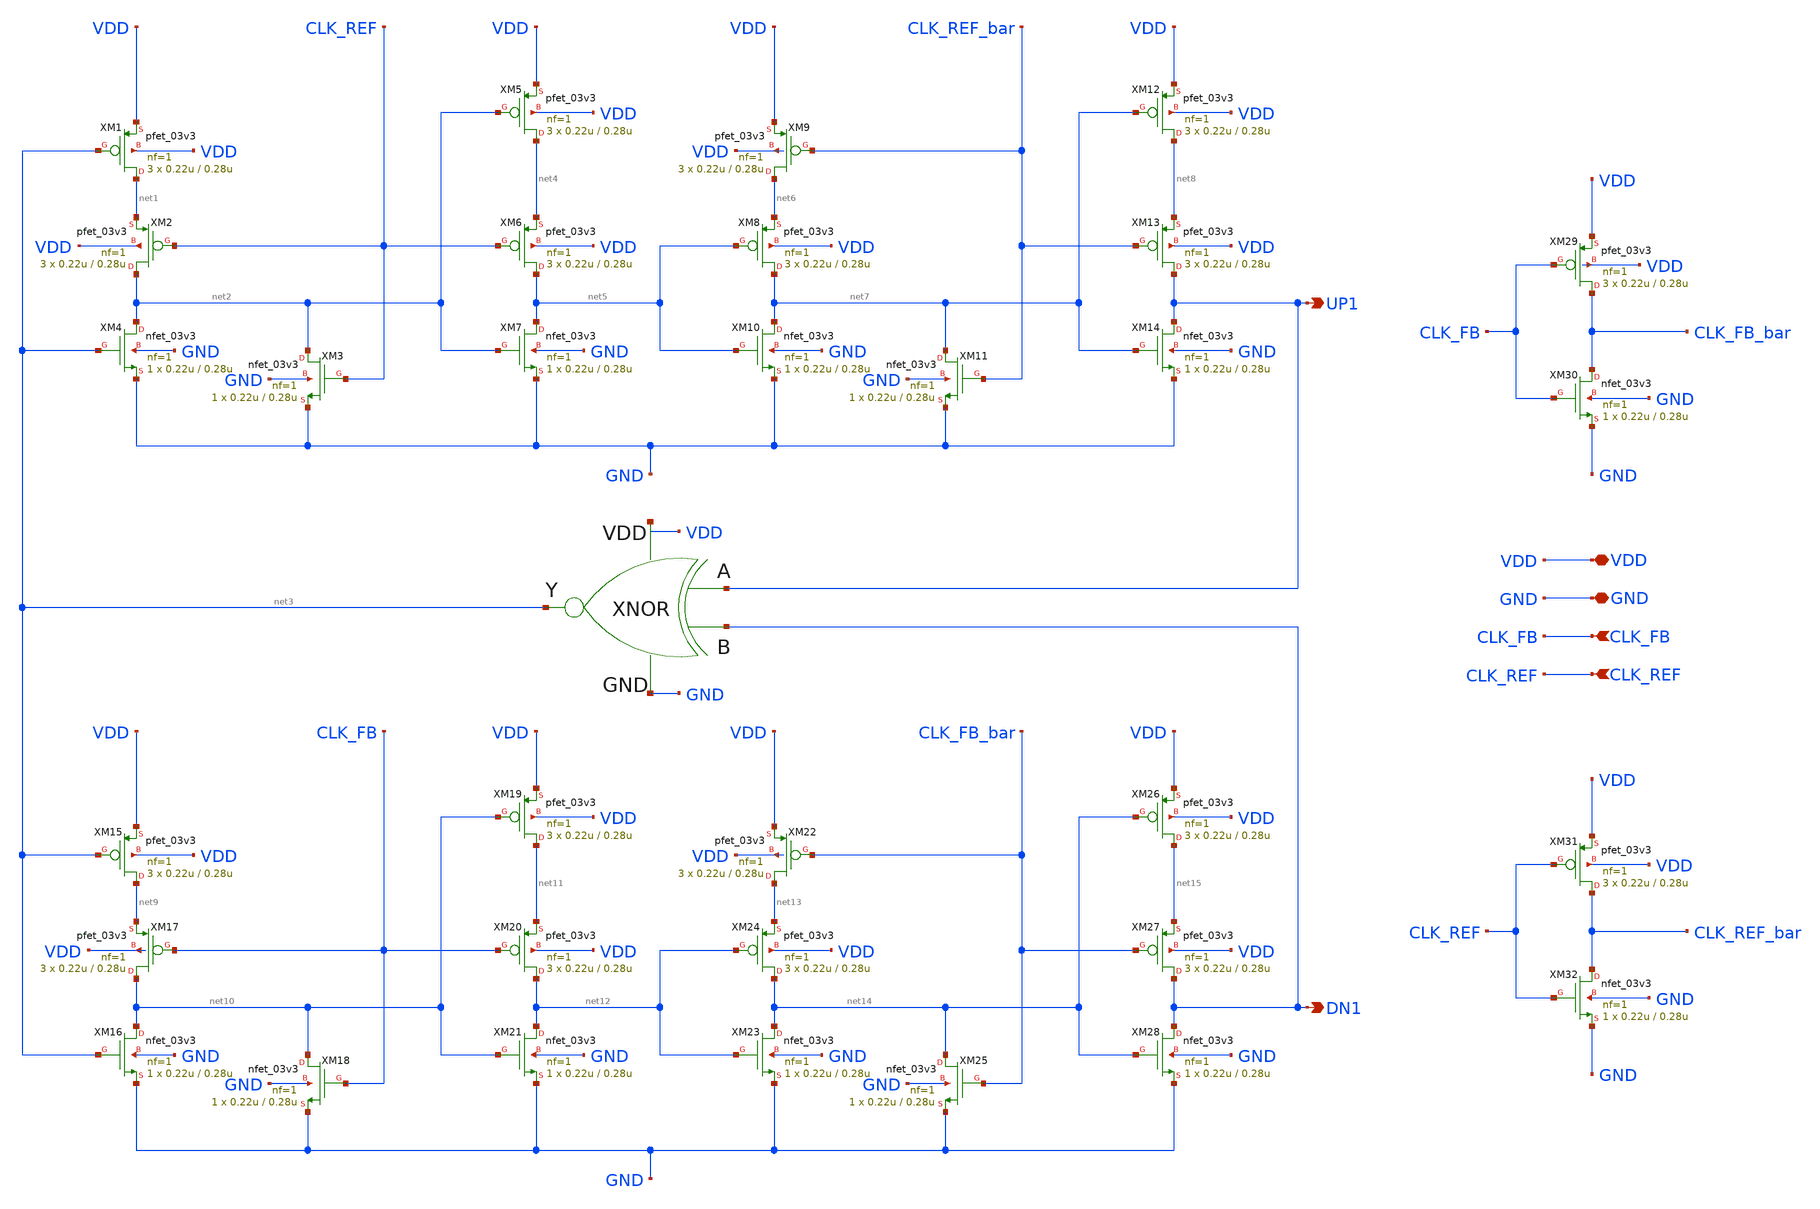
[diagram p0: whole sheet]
** sch_path: PFD/FTL_PFD.sch
**.subckt FTL_PFD UP1 DN1 CLK_FB CLK_REF VDD GND
*.opin UP1
*.opin DN1
*.ipin CLK_FB
*.ipin CLK_REF
*.iopin VDD
*.iopin GND
XM1 net1 net3 VDD VDD pfet_03v3 L=0.28u W=0.22u nf=1 ad='int((nf+1)/2) * W/nf * 0.18u' as='int((nf+2)/2) * W/nf * 0.18u'
+ pd='2*int((nf+1)/2) * (W/nf + 0.18u)' ps='2*int((nf+2)/2) * (W/nf + 0.18u)' nrd='0.18u / W' nrs='0.18u / W'
+ sa=0 sb=0 sd=0 m=3
XM4 net2 net3 GND GND nfet_03v3 L=0.28u W=0.22u nf=1 ad='int((nf+1)/2) * W/nf * 0.18u' as='int((nf+2)/2) * W/nf * 0.18u'
+ pd='2*int((nf+1)/2) * (W/nf + 0.18u)' ps='2*int((nf+2)/2) * (W/nf + 0.18u)' nrd='0.18u / W' nrs='0.18u / W'
+ sa=0 sb=0 sd=0 m=1
XM2 net2 CLK_REF net1 VDD pfet_03v3 L=0.28u W=0.22u nf=1 ad='int((nf+1)/2) * W/nf * 0.18u' as='int((nf+2)/2) * W/nf * 0.18u'
+ pd='2*int((nf+1)/2) * (W/nf + 0.18u)' ps='2*int((nf+2)/2) * (W/nf + 0.18u)' nrd='0.18u / W' nrs='0.18u / W'
+ sa=0 sb=0 sd=0 m=3
XM3 net2 CLK_REF GND GND nfet_03v3 L=0.28u W=0.22u nf=1 ad='int((nf+1)/2) * W/nf * 0.18u' as='int((nf+2)/2) * W/nf * 0.18u'
+ pd='2*int((nf+1)/2) * (W/nf + 0.18u)' ps='2*int((nf+2)/2) * (W/nf + 0.18u)' nrd='0.18u / W' nrs='0.18u / W'
+ sa=0 sb=0 sd=0 m=1
XM5 net4 net2 VDD VDD pfet_03v3 L=0.28u W=0.22u nf=1 ad='int((nf+1)/2) * W/nf * 0.18u' as='int((nf+2)/2) * W/nf * 0.18u'
+ pd='2*int((nf+1)/2) * (W/nf + 0.18u)' ps='2*int((nf+2)/2) * (W/nf + 0.18u)' nrd='0.18u / W' nrs='0.18u / W'
+ sa=0 sb=0 sd=0 m=3
XM6 net5 CLK_REF net4 VDD pfet_03v3 L=0.28u W=0.22u nf=1 ad='int((nf+1)/2) * W/nf * 0.18u' as='int((nf+2)/2) * W/nf * 0.18u'
+ pd='2*int((nf+1)/2) * (W/nf + 0.18u)' ps='2*int((nf+2)/2) * (W/nf + 0.18u)' nrd='0.18u / W' nrs='0.18u / W'
+ sa=0 sb=0 sd=0 m=3
XM7 net5 net2 GND GND nfet_03v3 L=0.28u W=0.22u nf=1 ad='int((nf+1)/2) * W/nf * 0.18u' as='int((nf+2)/2) * W/nf * 0.18u'
+ pd='2*int((nf+1)/2) * (W/nf + 0.18u)' ps='2*int((nf+2)/2) * (W/nf + 0.18u)' nrd='0.18u / W' nrs='0.18u / W'
+ sa=0 sb=0 sd=0 m=1
XM9 net6 CLK_REF_bar VDD VDD pfet_03v3 L=0.28u W=0.22u nf=1 ad='int((nf+1)/2) * W/nf * 0.18u' as='int((nf+2)/2) * W/nf * 0.18u'
+ pd='2*int((nf+1)/2) * (W/nf + 0.18u)' ps='2*int((nf+2)/2) * (W/nf + 0.18u)' nrd='0.18u / W' nrs='0.18u / W'
+ sa=0 sb=0 sd=0 m=3
XM10 net7 net5 GND GND nfet_03v3 L=0.28u W=0.22u nf=1 ad='int((nf+1)/2) * W/nf * 0.18u' as='int((nf+2)/2) * W/nf * 0.18u'
+ pd='2*int((nf+1)/2) * (W/nf + 0.18u)' ps='2*int((nf+2)/2) * (W/nf + 0.18u)' nrd='0.18u / W' nrs='0.18u / W'
+ sa=0 sb=0 sd=0 m=1
XM8 net7 net5 net6 VDD pfet_03v3 L=0.28u W=0.22u nf=1 ad='int((nf+1)/2) * W/nf * 0.18u' as='int((nf+2)/2) * W/nf * 0.18u'
+ pd='2*int((nf+1)/2) * (W/nf + 0.18u)' ps='2*int((nf+2)/2) * (W/nf + 0.18u)' nrd='0.18u / W' nrs='0.18u / W'
+ sa=0 sb=0 sd=0 m=3
XM11 net7 CLK_REF_bar GND GND nfet_03v3 L=0.28u W=0.22u nf=1 ad='int((nf+1)/2) * W/nf * 0.18u' as='int((nf+2)/2) * W/nf * 0.18u'
+ pd='2*int((nf+1)/2) * (W/nf + 0.18u)' ps='2*int((nf+2)/2) * (W/nf + 0.18u)' nrd='0.18u / W' nrs='0.18u / W'
+ sa=0 sb=0 sd=0 m=1
XM12 net8 net7 VDD VDD pfet_03v3 L=0.28u W=0.22u nf=1 ad='int((nf+1)/2) * W/nf * 0.18u' as='int((nf+2)/2) * W/nf * 0.18u'
+ pd='2*int((nf+1)/2) * (W/nf + 0.18u)' ps='2*int((nf+2)/2) * (W/nf + 0.18u)' nrd='0.18u / W' nrs='0.18u / W'
+ sa=0 sb=0 sd=0 m=3
XM13 UP1 CLK_REF_bar net8 VDD pfet_03v3 L=0.28u W=0.22u nf=1 ad='int((nf+1)/2) * W/nf * 0.18u' as='int((nf+2)/2) * W/nf * 0.18u'
+ pd='2*int((nf+1)/2) * (W/nf + 0.18u)' ps='2*int((nf+2)/2) * (W/nf + 0.18u)' nrd='0.18u / W' nrs='0.18u / W'
+ sa=0 sb=0 sd=0 m=3
XM14 UP1 net7 GND GND nfet_03v3 L=0.28u W=0.22u nf=1 ad='int((nf+1)/2) * W/nf * 0.18u' as='int((nf+2)/2) * W/nf * 0.18u'
+ pd='2*int((nf+1)/2) * (W/nf + 0.18u)' ps='2*int((nf+2)/2) * (W/nf + 0.18u)' nrd='0.18u / W' nrs='0.18u / W'
+ sa=0 sb=0 sd=0 m=1
XM15 net9 net3 VDD VDD pfet_03v3 L=0.28u W=0.22u nf=1 ad='int((nf+1)/2) * W/nf * 0.18u' as='int((nf+2)/2) * W/nf * 0.18u'
+ pd='2*int((nf+1)/2) * (W/nf + 0.18u)' ps='2*int((nf+2)/2) * (W/nf + 0.18u)' nrd='0.18u / W' nrs='0.18u / W'
+ sa=0 sb=0 sd=0 m=3
XM16 net10 net3 GND GND nfet_03v3 L=0.28u W=0.22u nf=1 ad='int((nf+1)/2) * W/nf * 0.18u' as='int((nf+2)/2) * W/nf * 0.18u'
+ pd='2*int((nf+1)/2) * (W/nf + 0.18u)' ps='2*int((nf+2)/2) * (W/nf + 0.18u)' nrd='0.18u / W' nrs='0.18u / W'
+ sa=0 sb=0 sd=0 m=1
XM17 net10 CLK_FB net9 VDD pfet_03v3 L=0.28u W=0.22u nf=1 ad='int((nf+1)/2) * W/nf * 0.18u' as='int((nf+2)/2) * W/nf * 0.18u'
+ pd='2*int((nf+1)/2) * (W/nf + 0.18u)' ps='2*int((nf+2)/2) * (W/nf + 0.18u)' nrd='0.18u / W' nrs='0.18u / W'
+ sa=0 sb=0 sd=0 m=3
XM18 net10 CLK_FB GND GND nfet_03v3 L=0.28u W=0.22u nf=1 ad='int((nf+1)/2) * W/nf * 0.18u' as='int((nf+2)/2) * W/nf * 0.18u'
+ pd='2*int((nf+1)/2) * (W/nf + 0.18u)' ps='2*int((nf+2)/2) * (W/nf + 0.18u)' nrd='0.18u / W' nrs='0.18u / W'
+ sa=0 sb=0 sd=0 m=1
XM19 net11 net10 VDD VDD pfet_03v3 L=0.28u W=0.22u nf=1 ad='int((nf+1)/2) * W/nf * 0.18u' as='int((nf+2)/2) * W/nf * 0.18u'
+ pd='2*int((nf+1)/2) * (W/nf + 0.18u)' ps='2*int((nf+2)/2) * (W/nf + 0.18u)' nrd='0.18u / W' nrs='0.18u / W'
+ sa=0 sb=0 sd=0 m=3
XM20 net12 CLK_FB net11 VDD pfet_03v3 L=0.28u W=0.22u nf=1 ad='int((nf+1)/2) * W/nf * 0.18u' as='int((nf+2)/2) * W/nf * 0.18u'
+ pd='2*int((nf+1)/2) * (W/nf + 0.18u)' ps='2*int((nf+2)/2) * (W/nf + 0.18u)' nrd='0.18u / W' nrs='0.18u / W'
+ sa=0 sb=0 sd=0 m=3
XM21 net12 net10 GND GND nfet_03v3 L=0.28u W=0.22u nf=1 ad='int((nf+1)/2) * W/nf * 0.18u' as='int((nf+2)/2) * W/nf * 0.18u'
+ pd='2*int((nf+1)/2) * (W/nf + 0.18u)' ps='2*int((nf+2)/2) * (W/nf + 0.18u)' nrd='0.18u / W' nrs='0.18u / W'
+ sa=0 sb=0 sd=0 m=1
XM22 net13 CLK_FB_bar VDD VDD pfet_03v3 L=0.28u W=0.22u nf=1 ad='int((nf+1)/2) * W/nf * 0.18u' as='int((nf+2)/2) * W/nf * 0.18u'
+ pd='2*int((nf+1)/2) * (W/nf + 0.18u)' ps='2*int((nf+2)/2) * (W/nf + 0.18u)' nrd='0.18u / W' nrs='0.18u / W'
+ sa=0 sb=0 sd=0 m=3
XM23 net14 net12 GND GND nfet_03v3 L=0.28u W=0.22u nf=1 ad='int((nf+1)/2) * W/nf * 0.18u' as='int((nf+2)/2) * W/nf * 0.18u'
+ pd='2*int((nf+1)/2) * (W/nf + 0.18u)' ps='2*int((nf+2)/2) * (W/nf + 0.18u)' nrd='0.18u / W' nrs='0.18u / W'
+ sa=0 sb=0 sd=0 m=1
XM24 net14 net12 net13 VDD pfet_03v3 L=0.28u W=0.22u nf=1 ad='int((nf+1)/2) * W/nf * 0.18u' as='int((nf+2)/2) * W/nf * 0.18u'
+ pd='2*int((nf+1)/2) * (W/nf + 0.18u)' ps='2*int((nf+2)/2) * (W/nf + 0.18u)' nrd='0.18u / W' nrs='0.18u / W'
+ sa=0 sb=0 sd=0 m=3
XM25 net14 CLK_FB_bar GND GND nfet_03v3 L=0.28u W=0.22u nf=1 ad='int((nf+1)/2) * W/nf * 0.18u' as='int((nf+2)/2) * W/nf * 0.18u'
+ pd='2*int((nf+1)/2) * (W/nf + 0.18u)' ps='2*int((nf+2)/2) * (W/nf + 0.18u)' nrd='0.18u / W' nrs='0.18u / W'
+ sa=0 sb=0 sd=0 m=1
XM26 net15 net14 VDD VDD pfet_03v3 L=0.28u W=0.22u nf=1 ad='int((nf+1)/2) * W/nf * 0.18u' as='int((nf+2)/2) * W/nf * 0.18u'
+ pd='2*int((nf+1)/2) * (W/nf + 0.18u)' ps='2*int((nf+2)/2) * (W/nf + 0.18u)' nrd='0.18u / W' nrs='0.18u / W'
+ sa=0 sb=0 sd=0 m=3
XM27 DN1 CLK_FB_bar net15 VDD pfet_03v3 L=0.28u W=0.22u nf=1 ad='int((nf+1)/2) * W/nf * 0.18u' as='int((nf+2)/2) * W/nf * 0.18u'
+ pd='2*int((nf+1)/2) * (W/nf + 0.18u)' ps='2*int((nf+2)/2) * (W/nf + 0.18u)' nrd='0.18u / W' nrs='0.18u / W'
+ sa=0 sb=0 sd=0 m=3
XM28 DN1 net14 GND GND nfet_03v3 L=0.28u W=0.22u nf=1 ad='int((nf+1)/2) * W/nf * 0.18u' as='int((nf+2)/2) * W/nf * 0.18u'
+ pd='2*int((nf+1)/2) * (W/nf + 0.18u)' ps='2*int((nf+2)/2) * (W/nf + 0.18u)' nrd='0.18u / W' nrs='0.18u / W'
+ sa=0 sb=0 sd=0 m=1
x1 GND UP1 DN1 net16 net3 XNOR
XM29 CLK_FB_bar CLK_FB VDD VDD pfet_03v3 L=0.28u W=0.22u nf=1 ad='int((nf+1)/2) * W/nf * 0.18u' as='int((nf+2)/2) * W/nf * 0.18u'
+ pd='2*int((nf+1)/2) * (W/nf + 0.18u)' ps='2*int((nf+2)/2) * (W/nf + 0.18u)' nrd='0.18u / W' nrs='0.18u / W'
+ sa=0 sb=0 sd=0 m=3
XM30 CLK_FB_bar CLK_FB GND GND nfet_03v3 L=0.28u W=0.22u nf=1 ad='int((nf+1)/2) * W/nf * 0.18u' as='int((nf+2)/2) * W/nf * 0.18u'
+ pd='2*int((nf+1)/2) * (W/nf + 0.18u)' ps='2*int((nf+2)/2) * (W/nf + 0.18u)' nrd='0.18u / W' nrs='0.18u / W'
+ sa=0 sb=0 sd=0 m=1
XM31 CLK_REF_bar CLK_REF VDD VDD pfet_03v3 L=0.28u W=0.22u nf=1 ad='int((nf+1)/2) * W/nf * 0.18u' as='int((nf+2)/2) * W/nf * 0.18u'
+ pd='2*int((nf+1)/2) * (W/nf + 0.18u)' ps='2*int((nf+2)/2) * (W/nf + 0.18u)' nrd='0.18u / W' nrs='0.18u / W'
+ sa=0 sb=0 sd=0 m=3
XM32 CLK_REF_bar CLK_REF GND GND nfet_03v3 L=0.28u W=0.22u nf=1 ad='int((nf+1)/2) * W/nf * 0.18u' as='int((nf+2)/2) * W/nf * 0.18u'
+ pd='2*int((nf+1)/2) * (W/nf + 0.18u)' ps='2*int((nf+2)/2) * (W/nf + 0.18u)' nrd='0.18u / W' nrs='0.18u / W'
+ sa=0 sb=0 sd=0 m=1
**.ends

* expanding   symbol:  XNOR.sym # of pins=5
** sym_path: PFD/XNOR.sym
** sch_path: PFD/XNOR.sch
.subckt XNOR GND A B VDD Y
*.opin Y
*.ipin A
*.ipin B
*.iopin VDD
*.iopin GND
XM1 net1 A VDD VDD pfet_03v3 L=0.28u W=0.22u nf=1 ad='int((nf+1)/2) * W/nf * 0.18u' as='int((nf+2)/2) * W/nf * 0.18u'
+ pd='2*int((nf+1)/2) * (W/nf + 0.18u)' ps='2*int((nf+2)/2) * (W/nf + 0.18u)' nrd='0.18u / W' nrs='0.18u / W'
+ sa=0 sb=0 sd=0 m=3
XM2 Y A_bar net1 VDD pfet_03v3 L=0.28u W=0.22u nf=1 ad='int((nf+1)/2) * W/nf * 0.18u' as='int((nf+2)/2) * W/nf * 0.18u'
+ pd='2*int((nf+1)/2) * (W/nf + 0.18u)' ps='2*int((nf+2)/2) * (W/nf + 0.18u)' nrd='0.18u / W' nrs='0.18u / W'
+ sa=0 sb=0 sd=0 m=3
XM3 Y B_bar net2 GND nfet_03v3 L=0.28u W=0.22u nf=1 ad='int((nf+1)/2) * W/nf * 0.18u' as='int((nf+2)/2) * W/nf * 0.18u'
+ pd='2*int((nf+1)/2) * (W/nf + 0.18u)' ps='2*int((nf+2)/2) * (W/nf + 0.18u)' nrd='0.18u / W' nrs='0.18u / W'
+ sa=0 sb=0 sd=0 m=1
XM4 net2 A GND GND nfet_03v3 L=0.28u W=0.22u nf=1 ad='int((nf+1)/2) * W/nf * 0.18u' as='int((nf+2)/2) * W/nf * 0.18u'
+ pd='2*int((nf+1)/2) * (W/nf + 0.18u)' ps='2*int((nf+2)/2) * (W/nf + 0.18u)' nrd='0.18u / W' nrs='0.18u / W'
+ sa=0 sb=0 sd=0 m=1
XM5 net3 B_bar VDD VDD pfet_03v3 L=0.28u W=0.22u nf=1 ad='int((nf+1)/2) * W/nf * 0.18u' as='int((nf+2)/2) * W/nf * 0.18u'
+ pd='2*int((nf+1)/2) * (W/nf + 0.18u)' ps='2*int((nf+2)/2) * (W/nf + 0.18u)' nrd='0.18u / W' nrs='0.18u / W'
+ sa=0 sb=0 sd=0 m=3
XM6 Y B net3 VDD pfet_03v3 L=0.28u W=0.22u nf=1 ad='int((nf+1)/2) * W/nf * 0.18u' as='int((nf+2)/2) * W/nf * 0.18u'
+ pd='2*int((nf+1)/2) * (W/nf + 0.18u)' ps='2*int((nf+2)/2) * (W/nf + 0.18u)' nrd='0.18u / W' nrs='0.18u / W'
+ sa=0 sb=0 sd=0 m=3
XM7 Y A_bar net4 GND nfet_03v3 L=0.28u W=0.22u nf=1 ad='int((nf+1)/2) * W/nf * 0.18u' as='int((nf+2)/2) * W/nf * 0.18u'
+ pd='2*int((nf+1)/2) * (W/nf + 0.18u)' ps='2*int((nf+2)/2) * (W/nf + 0.18u)' nrd='0.18u / W' nrs='0.18u / W'
+ sa=0 sb=0 sd=0 m=1
XM8 net4 B GND GND nfet_03v3 L=0.28u W=0.22u nf=1 ad='int((nf+1)/2) * W/nf * 0.18u' as='int((nf+2)/2) * W/nf * 0.18u'
+ pd='2*int((nf+1)/2) * (W/nf + 0.18u)' ps='2*int((nf+2)/2) * (W/nf + 0.18u)' nrd='0.18u / W' nrs='0.18u / W'
+ sa=0 sb=0 sd=0 m=1
XM9 A_bar A VDD VDD pfet_03v3 L=0.28u W=0.22u nf=1 ad='int((nf+1)/2) * W/nf * 0.18u' as='int((nf+2)/2) * W/nf * 0.18u'
+ pd='2*int((nf+1)/2) * (W/nf + 0.18u)' ps='2*int((nf+2)/2) * (W/nf + 0.18u)' nrd='0.18u / W' nrs='0.18u / W'
+ sa=0 sb=0 sd=0 m=3
XM10 A_bar A GND GND nfet_03v3 L=0.28u W=0.22u nf=1 ad='int((nf+1)/2) * W/nf * 0.18u' as='int((nf+2)/2) * W/nf * 0.18u'
+ pd='2*int((nf+1)/2) * (W/nf + 0.18u)' ps='2*int((nf+2)/2) * (W/nf + 0.18u)' nrd='0.18u / W' nrs='0.18u / W'
+ sa=0 sb=0 sd=0 m=1
XM11 B_bar B VDD VDD pfet_03v3 L=0.28u W=0.22u nf=1 ad='int((nf+1)/2) * W/nf * 0.18u' as='int((nf+2)/2) * W/nf * 0.18u'
+ pd='2*int((nf+1)/2) * (W/nf + 0.18u)' ps='2*int((nf+2)/2) * (W/nf + 0.18u)' nrd='0.18u / W' nrs='0.18u / W'
+ sa=0 sb=0 sd=0 m=3
XM12 B_bar B GND GND nfet_03v3 L=0.28u W=0.22u nf=1 ad='int((nf+1)/2) * W/nf * 0.18u' as='int((nf+2)/2) * W/nf * 0.18u'
+ pd='2*int((nf+1)/2) * (W/nf + 0.18u)' ps='2*int((nf+2)/2) * (W/nf + 0.18u)' nrd='0.18u / W' nrs='0.18u / W'
+ sa=0 sb=0 sd=0 m=1
.ends

.end
